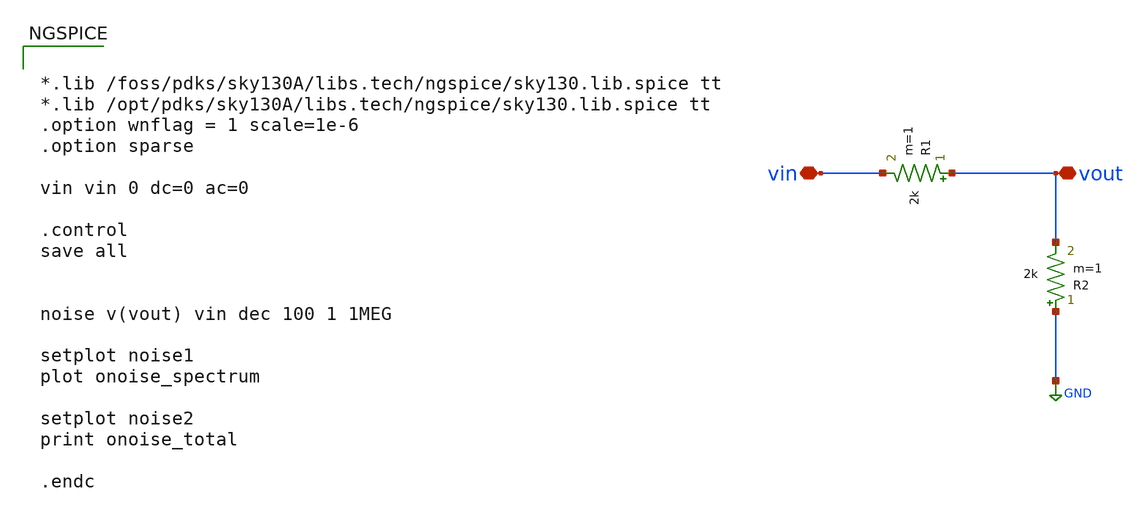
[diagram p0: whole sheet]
** sch_path: xschem/Tareas/Tarea_2/resistor-noise_jm.sch
**.subckt resistor-noise_jm vin vout
*.iopin vin
*.iopin vout
R1 vout vin 2k m=1
R2 GND vout 2k m=1
**** begin user architecture code


*.lib /foss/pdks/sky130A/libs.tech/ngspice/sky130.lib.spice tt
*.lib /opt/pdks/sky130A/libs.tech/ngspice/sky130.lib.spice tt
.option wnflag = 1 scale=1e-6
.option sparse

vin vin 0 dc=0 ac=0

.control
save all


noise v(vout) vin dec 100 1 1MEG

setplot noise1
plot onoise_spectrum

setplot noise2
print onoise_total

.endc


**** end user architecture code
**.ends
.GLOBAL GND
.end
